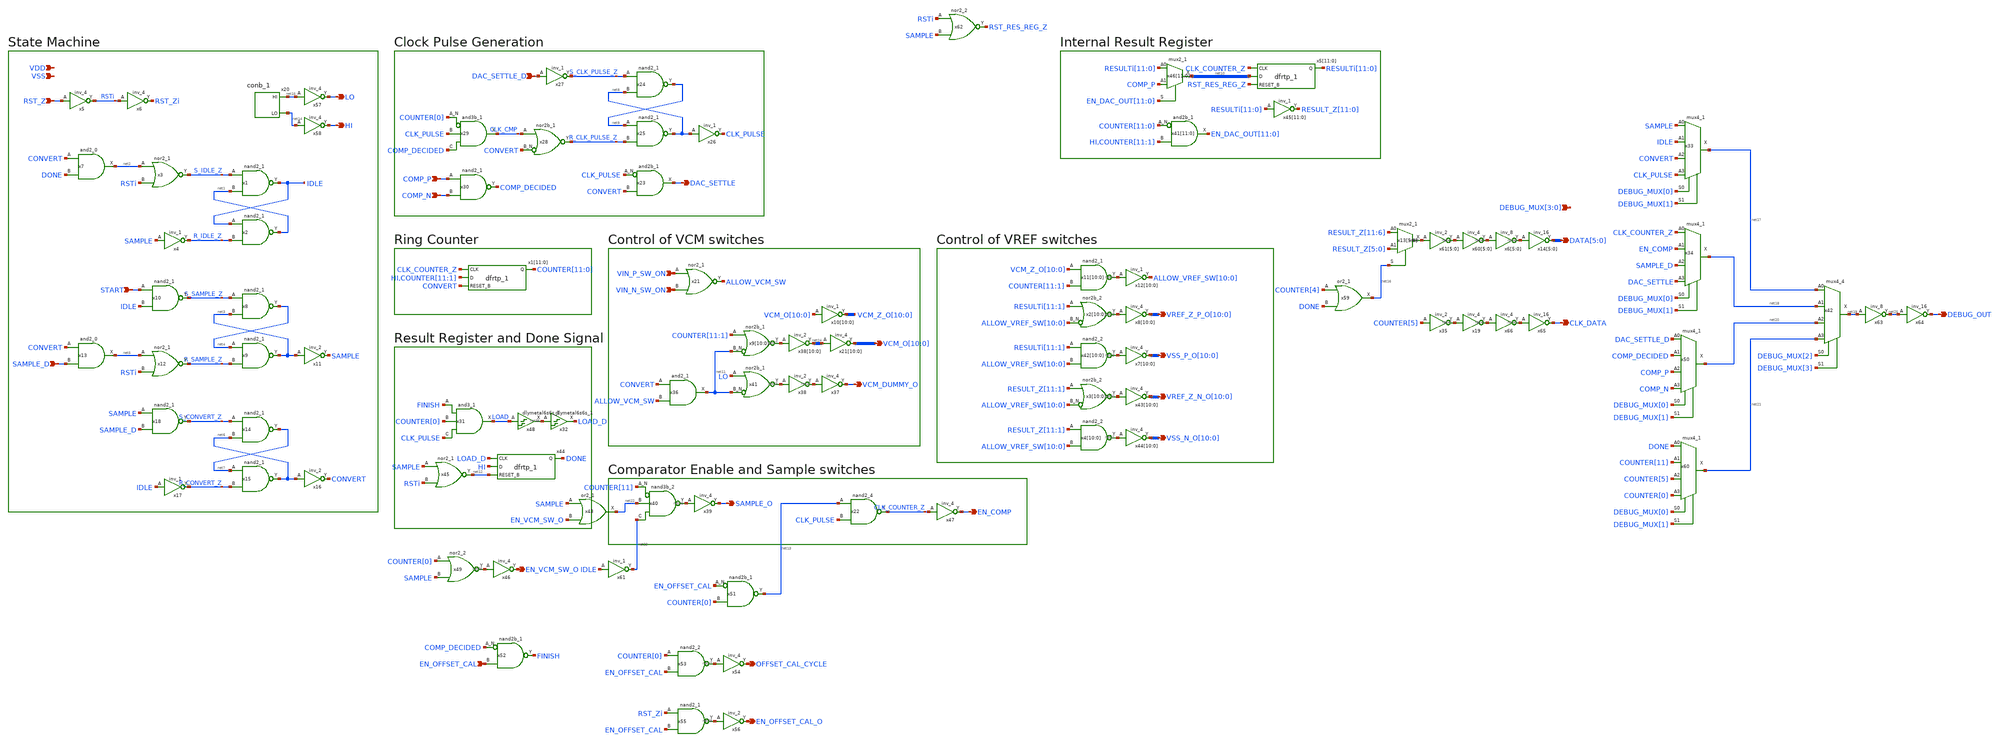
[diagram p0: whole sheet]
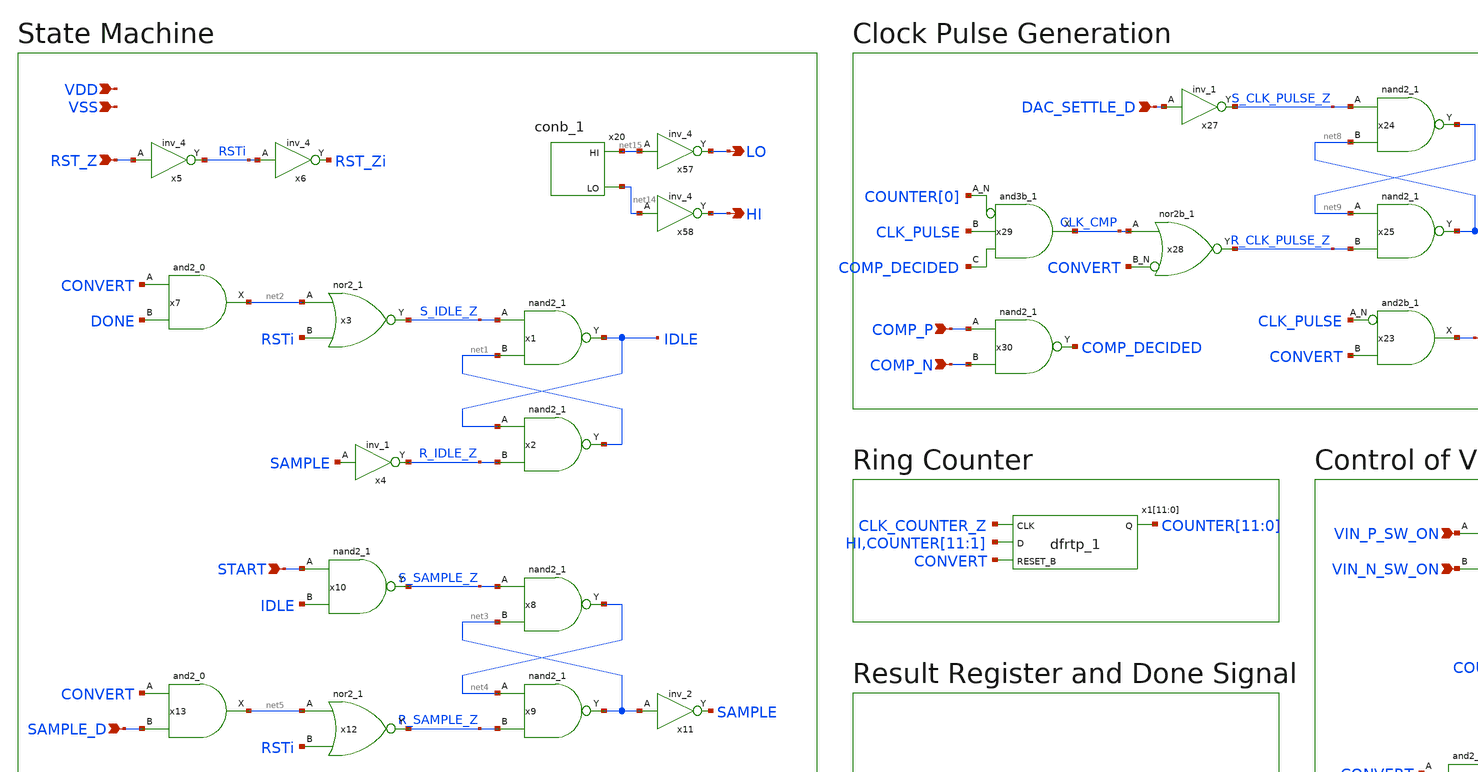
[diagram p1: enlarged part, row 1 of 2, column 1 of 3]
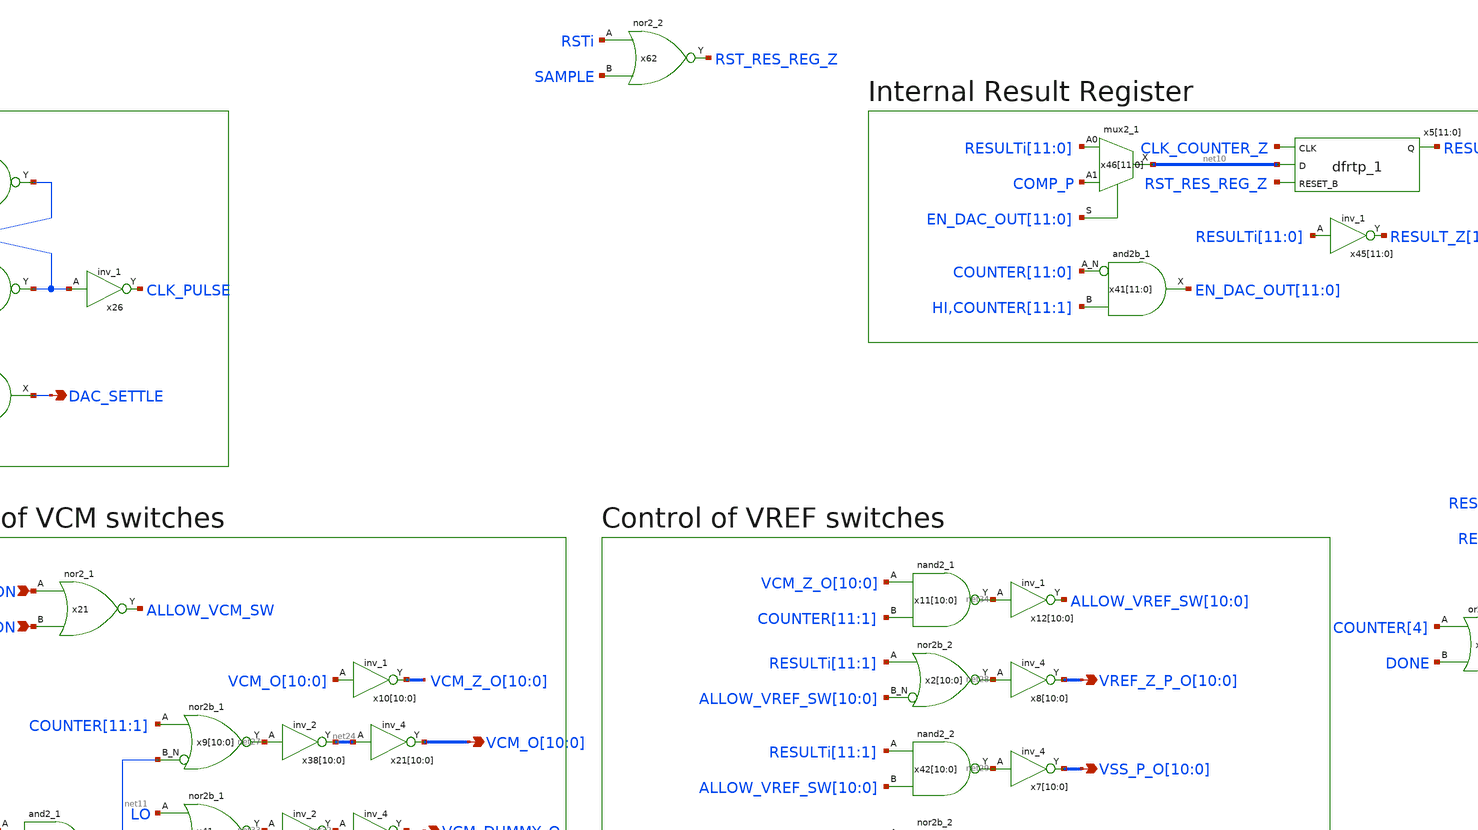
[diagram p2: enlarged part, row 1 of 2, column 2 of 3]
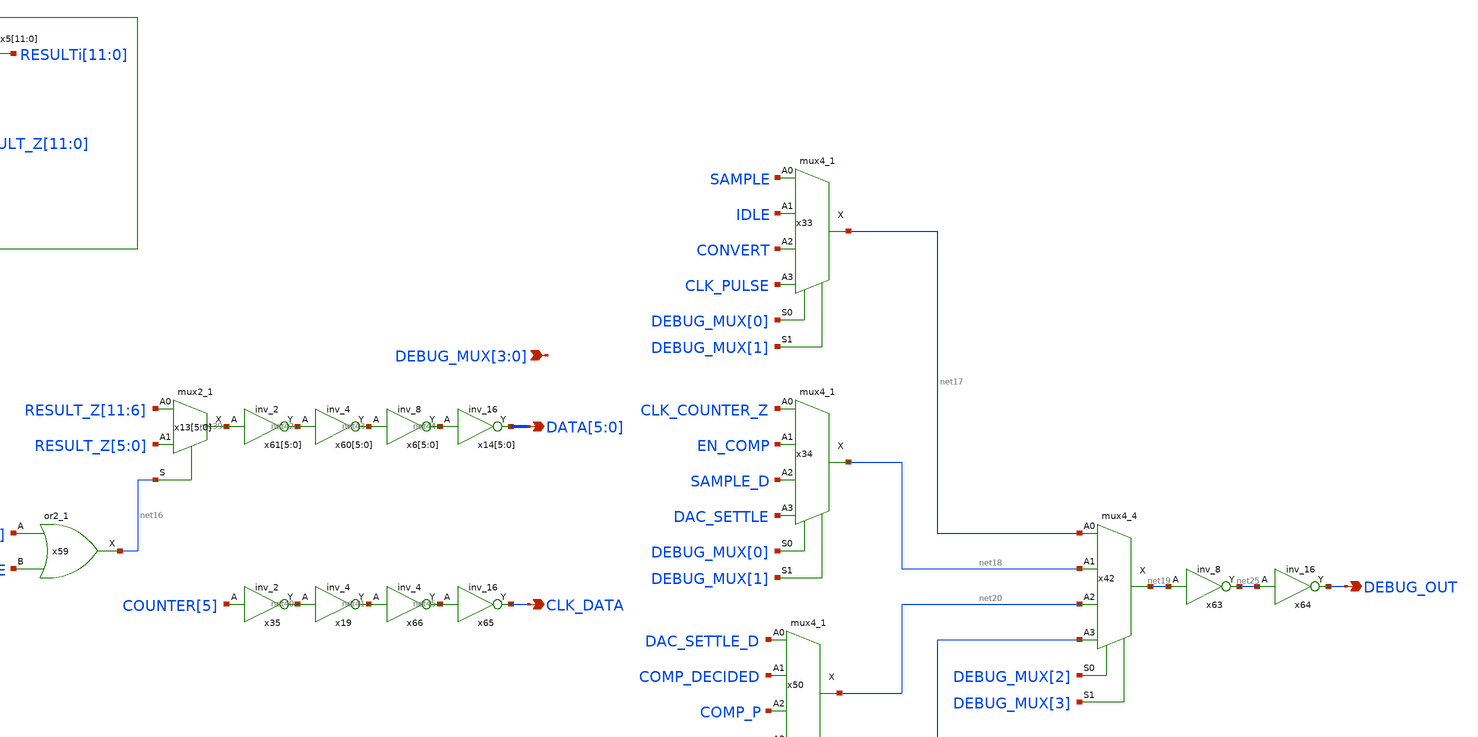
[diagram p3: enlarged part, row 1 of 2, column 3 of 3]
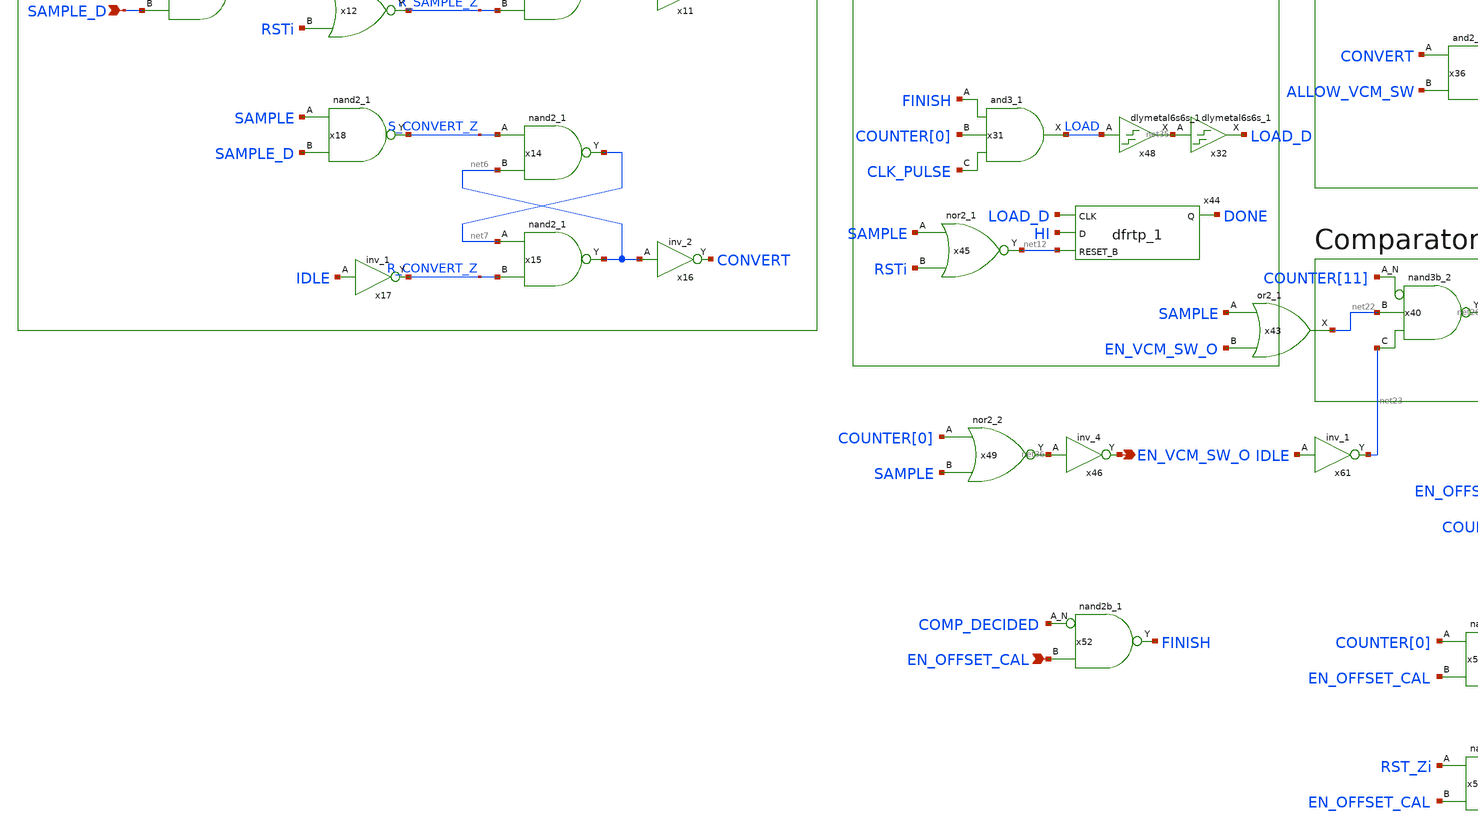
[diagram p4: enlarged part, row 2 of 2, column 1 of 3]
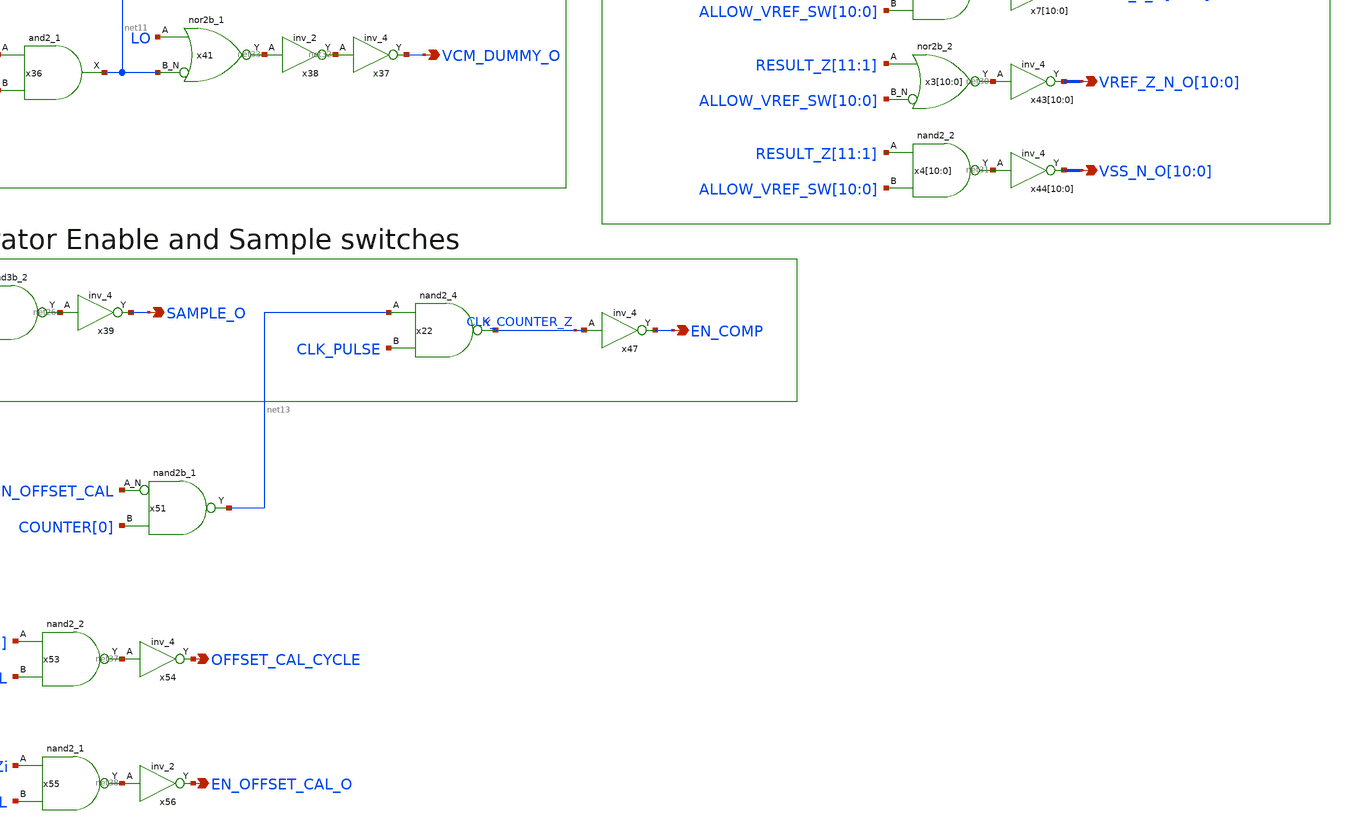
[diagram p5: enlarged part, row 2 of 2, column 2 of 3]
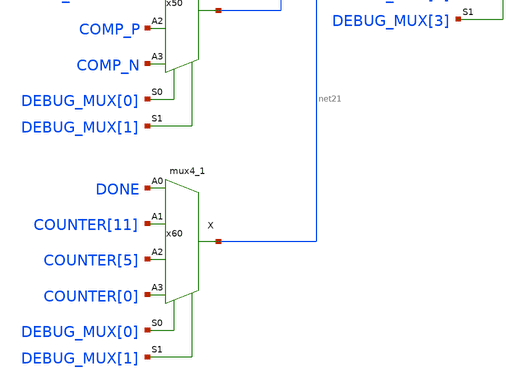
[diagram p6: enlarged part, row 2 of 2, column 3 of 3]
** sch_path: state_machine/openlane_backup/state_machine.sch
**.subckt state_machine RST_Z START COMP_P COMP_N SAMPLE_O
*+ VCM_O[10],VCM_O[9],VCM_O[8],VCM_O[7],VCM_O[6],VCM_O[5],VCM_O[4],VCM_O[3],VCM_O[2],VCM_O[1],VCM_O[0] EN_COMP VDD VSS VIN_P_SW_ON VIN_N_SW_ON VCM_DUMMY_O HI LO EN_VCM_SW_O EN_OFFSET_CAL
*+ OFFSET_CAL_CYCLE EN_OFFSET_CAL_O DAC_SETTLE DAC_SETTLE_D SAMPLE_D CLK_DATA
*+ DATA[5],DATA[4],DATA[3],DATA[2],DATA[1],DATA[0] DEBUG_OUT DEBUG_MUX[3],DEBUG_MUX[2],DEBUG_MUX[1],DEBUG_MUX[0]
*+ VREF_Z_P_O[10],VREF_Z_P_O[9],VREF_Z_P_O[8],VREF_Z_P_O[7],VREF_Z_P_O[6],VREF_Z_P_O[5],VREF_Z_P_O[4],VREF_Z_P_O[3],VREF_Z_P_O[2],VREF_Z_P_O[1],VREF_Z_P_O[0]
*+ VSS_P_O[10],VSS_P_O[9],VSS_P_O[8],VSS_P_O[7],VSS_P_O[6],VSS_P_O[5],VSS_P_O[4],VSS_P_O[3],VSS_P_O[2],VSS_P_O[1],VSS_P_O[0]
*+ VREF_Z_N_O[10],VREF_Z_N_O[9],VREF_Z_N_O[8],VREF_Z_N_O[7],VREF_Z_N_O[6],VREF_Z_N_O[5],VREF_Z_N_O[4],VREF_Z_N_O[3],VREF_Z_N_O[2],VREF_Z_N_O[1],VREF_Z_N_O[0]
*+ VSS_N_O[10],VSS_N_O[9],VSS_N_O[8],VSS_N_O[7],VSS_N_O[6],VSS_N_O[5],VSS_N_O[4],VSS_N_O[3],VSS_N_O[2],VSS_N_O[1],VSS_N_O[0]
*.ipin RST_Z
*.ipin START
*.ipin COMP_P
*.ipin COMP_N
*.opin SAMPLE_O
*.opin
*+ VCM_O[10],VCM_O[9],VCM_O[8],VCM_O[7],VCM_O[6],VCM_O[5],VCM_O[4],VCM_O[3],VCM_O[2],VCM_O[1],VCM_O[0]
*.opin EN_COMP
*.ipin VDD
*.ipin VSS
*.ipin VIN_P_SW_ON
*.ipin VIN_N_SW_ON
*.opin VCM_DUMMY_O
*.opin HI
*.opin LO
*.opin EN_VCM_SW_O
*.ipin EN_OFFSET_CAL
*.opin OFFSET_CAL_CYCLE
*.opin EN_OFFSET_CAL_O
*.opin DAC_SETTLE
*.ipin DAC_SETTLE_D
*.ipin SAMPLE_D
*.opin CLK_DATA
*.opin DATA[5],DATA[4],DATA[3],DATA[2],DATA[1],DATA[0]
*.opin DEBUG_OUT
*.ipin DEBUG_MUX[3],DEBUG_MUX[2],DEBUG_MUX[1],DEBUG_MUX[0]
*.opin
*+ VREF_Z_P_O[10],VREF_Z_P_O[9],VREF_Z_P_O[8],VREF_Z_P_O[7],VREF_Z_P_O[6],VREF_Z_P_O[5],VREF_Z_P_O[4],VREF_Z_P_O[3],VREF_Z_P_O[2],VREF_Z_P_O[1],VREF_Z_P_O[0]
*.opin
*+ VSS_P_O[10],VSS_P_O[9],VSS_P_O[8],VSS_P_O[7],VSS_P_O[6],VSS_P_O[5],VSS_P_O[4],VSS_P_O[3],VSS_P_O[2],VSS_P_O[1],VSS_P_O[0]
*.opin
*+ VREF_Z_N_O[10],VREF_Z_N_O[9],VREF_Z_N_O[8],VREF_Z_N_O[7],VREF_Z_N_O[6],VREF_Z_N_O[5],VREF_Z_N_O[4],VREF_Z_N_O[3],VREF_Z_N_O[2],VREF_Z_N_O[1],VREF_Z_N_O[0]
*.opin
*+ VSS_N_O[10],VSS_N_O[9],VSS_N_O[8],VSS_N_O[7],VSS_N_O[6],VSS_N_O[5],VSS_N_O[4],VSS_N_O[3],VSS_N_O[2],VSS_N_O[1],VSS_N_O[0]
x1 S_IDLE_Z net1 VSS VSS VDD VDD IDLE sky130_fd_sc_hd__nand2_1
x3 net2 RSTi VSS VSS VDD VDD S_IDLE_Z sky130_fd_sc_hd__nor2_1
x2 IDLE R_IDLE_Z VSS VSS VDD VDD net1 sky130_fd_sc_hd__nand2_1
x4 SAMPLE VSS VSS VDD VDD R_IDLE_Z sky130_fd_sc_hd__inv_1
x5 RST_Z VSS VSS VDD VDD RSTi sky130_fd_sc_hd__inv_4
x6 RSTi VSS VSS VDD VDD RST_Zi sky130_fd_sc_hd__inv_4
x7 CONVERT DONE VSS VSS VDD VDD net2 sky130_fd_sc_hd__and2_0
x8 S_SAMPLE_Z net3 VSS VSS VDD VDD net4 sky130_fd_sc_hd__nand2_1
x9 net4 R_SAMPLE_Z VSS VSS VDD VDD net3 sky130_fd_sc_hd__nand2_1
x10 START IDLE VSS VSS VDD VDD S_SAMPLE_Z sky130_fd_sc_hd__nand2_1
x11 net3 VSS VSS VDD VDD SAMPLE sky130_fd_sc_hd__inv_2
x12 net5 RSTi VSS VSS VDD VDD R_SAMPLE_Z sky130_fd_sc_hd__nor2_1
x13 CONVERT SAMPLE_D VSS VSS VDD VDD net5 sky130_fd_sc_hd__and2_0
x14 S_CONVERT_Z net6 VSS VSS VDD VDD net7 sky130_fd_sc_hd__nand2_1
x15 net7 R_CONVERT_Z VSS VSS VDD VDD net6 sky130_fd_sc_hd__nand2_1
x16 net6 VSS VSS VDD VDD CONVERT sky130_fd_sc_hd__inv_2
x17 IDLE VSS VSS VDD VDD R_CONVERT_Z sky130_fd_sc_hd__inv_1
x20 VSS VSS VDD VDD net15 net14 sky130_fd_sc_hd__conb_1
x23 CLK_PULSE CONVERT VSS VSS VDD VDD DAC_SETTLE sky130_fd_sc_hd__and2b_1
x24 S_CLK_PULSE_Z net8 VSS VSS VDD VDD net9 sky130_fd_sc_hd__nand2_1
x25 net9 R_CLK_PULSE_Z VSS VSS VDD VDD net8 sky130_fd_sc_hd__nand2_1
x26 net8 VSS VSS VDD VDD CLK_PULSE sky130_fd_sc_hd__inv_1
x27 DAC_SETTLE_D VSS VSS VDD VDD S_CLK_PULSE_Z sky130_fd_sc_hd__inv_1
x28 CLK_CMP CONVERT VSS VSS VDD VDD R_CLK_PULSE_Z sky130_fd_sc_hd__nor2b_1
x29 COUNTER[0] CLK_PULSE COMP_DECIDED VSS VSS VDD VDD CLK_CMP sky130_fd_sc_hd__and3b_1
x30 COMP_P COMP_N VSS VSS VDD VDD COMP_DECIDED sky130_fd_sc_hd__nand2_1
x39 net26 VSS VSS VDD VDD SAMPLE_O sky130_fd_sc_hd__inv_4
x40 COUNTER[11] net22 net23 VSS VSS VDD VDD net26 sky130_fd_sc_hd__nand3b_2
x1[11] CLK_COUNTER_Z HI CONVERT VSS VSS VDD VDD COUNTER[11] sky130_fd_sc_hd__dfrtp_1
x1[10] CLK_COUNTER_Z COUNTER[11] CONVERT VSS VSS VDD VDD COUNTER[10] sky130_fd_sc_hd__dfrtp_1
x1[9] CLK_COUNTER_Z COUNTER[10] CONVERT VSS VSS VDD VDD COUNTER[9] sky130_fd_sc_hd__dfrtp_1
x1[8] CLK_COUNTER_Z COUNTER[9] CONVERT VSS VSS VDD VDD COUNTER[8] sky130_fd_sc_hd__dfrtp_1
x1[7] CLK_COUNTER_Z COUNTER[8] CONVERT VSS VSS VDD VDD COUNTER[7] sky130_fd_sc_hd__dfrtp_1
x1[6] CLK_COUNTER_Z COUNTER[7] CONVERT VSS VSS VDD VDD COUNTER[6] sky130_fd_sc_hd__dfrtp_1
x1[5] CLK_COUNTER_Z COUNTER[6] CONVERT VSS VSS VDD VDD COUNTER[5] sky130_fd_sc_hd__dfrtp_1
x1[4] CLK_COUNTER_Z COUNTER[5] CONVERT VSS VSS VDD VDD COUNTER[4] sky130_fd_sc_hd__dfrtp_1
x1[3] CLK_COUNTER_Z COUNTER[4] CONVERT VSS VSS VDD VDD COUNTER[3] sky130_fd_sc_hd__dfrtp_1
x1[2] CLK_COUNTER_Z COUNTER[3] CONVERT VSS VSS VDD VDD COUNTER[2] sky130_fd_sc_hd__dfrtp_1
x1[1] CLK_COUNTER_Z COUNTER[2] CONVERT VSS VSS VDD VDD COUNTER[1] sky130_fd_sc_hd__dfrtp_1
x1[0] CLK_COUNTER_Z COUNTER[1] CONVERT VSS VSS VDD VDD COUNTER[0] sky130_fd_sc_hd__dfrtp_1
x21[10] net24[10] VSS VSS VDD VDD VCM_O[10] sky130_fd_sc_hd__inv_4
x21[9] net24[9] VSS VSS VDD VDD VCM_O[9] sky130_fd_sc_hd__inv_4
x21[8] net24[8] VSS VSS VDD VDD VCM_O[8] sky130_fd_sc_hd__inv_4
x21[7] net24[7] VSS VSS VDD VDD VCM_O[7] sky130_fd_sc_hd__inv_4
x21[6] net24[6] VSS VSS VDD VDD VCM_O[6] sky130_fd_sc_hd__inv_4
x21[5] net24[5] VSS VSS VDD VDD VCM_O[5] sky130_fd_sc_hd__inv_4
x21[4] net24[4] VSS VSS VDD VDD VCM_O[4] sky130_fd_sc_hd__inv_4
x21[3] net24[3] VSS VSS VDD VDD VCM_O[3] sky130_fd_sc_hd__inv_4
x21[2] net24[2] VSS VSS VDD VDD VCM_O[2] sky130_fd_sc_hd__inv_4
x21[1] net24[1] VSS VSS VDD VDD VCM_O[1] sky130_fd_sc_hd__inv_4
x21[0] net24[0] VSS VSS VDD VDD VCM_O[0] sky130_fd_sc_hd__inv_4
x38[10] net27[10] VSS VSS VDD VDD net24[10] sky130_fd_sc_hd__inv_2
x38[9] net27[9] VSS VSS VDD VDD net24[9] sky130_fd_sc_hd__inv_2
x38[8] net27[8] VSS VSS VDD VDD net24[8] sky130_fd_sc_hd__inv_2
x38[7] net27[7] VSS VSS VDD VDD net24[7] sky130_fd_sc_hd__inv_2
x38[6] net27[6] VSS VSS VDD VDD net24[6] sky130_fd_sc_hd__inv_2
x38[5] net27[5] VSS VSS VDD VDD net24[5] sky130_fd_sc_hd__inv_2
x38[4] net27[4] VSS VSS VDD VDD net24[4] sky130_fd_sc_hd__inv_2
x38[3] net27[3] VSS VSS VDD VDD net24[3] sky130_fd_sc_hd__inv_2
x38[2] net27[2] VSS VSS VDD VDD net24[2] sky130_fd_sc_hd__inv_2
x38[1] net27[1] VSS VSS VDD VDD net24[1] sky130_fd_sc_hd__inv_2
x38[0] net27[0] VSS VSS VDD VDD net24[0] sky130_fd_sc_hd__inv_2
x41[11] COUNTER[11] HI VSS VSS VDD VDD EN_DAC_OUT[11] sky130_fd_sc_hd__and2b_1
x41[10] COUNTER[10] COUNTER[11] VSS VSS VDD VDD EN_DAC_OUT[10] sky130_fd_sc_hd__and2b_1
x41[9] COUNTER[9] COUNTER[10] VSS VSS VDD VDD EN_DAC_OUT[9] sky130_fd_sc_hd__and2b_1
x41[8] COUNTER[8] COUNTER[9] VSS VSS VDD VDD EN_DAC_OUT[8] sky130_fd_sc_hd__and2b_1
x41[7] COUNTER[7] COUNTER[8] VSS VSS VDD VDD EN_DAC_OUT[7] sky130_fd_sc_hd__and2b_1
x41[6] COUNTER[6] COUNTER[7] VSS VSS VDD VDD EN_DAC_OUT[6] sky130_fd_sc_hd__and2b_1
x41[5] COUNTER[5] COUNTER[6] VSS VSS VDD VDD EN_DAC_OUT[5] sky130_fd_sc_hd__and2b_1
x41[4] COUNTER[4] COUNTER[5] VSS VSS VDD VDD EN_DAC_OUT[4] sky130_fd_sc_hd__and2b_1
x41[3] COUNTER[3] COUNTER[4] VSS VSS VDD VDD EN_DAC_OUT[3] sky130_fd_sc_hd__and2b_1
x41[2] COUNTER[2] COUNTER[3] VSS VSS VDD VDD EN_DAC_OUT[2] sky130_fd_sc_hd__and2b_1
x41[1] COUNTER[1] COUNTER[2] VSS VSS VDD VDD EN_DAC_OUT[1] sky130_fd_sc_hd__and2b_1
x41[0] COUNTER[0] COUNTER[1] VSS VSS VDD VDD EN_DAC_OUT[0] sky130_fd_sc_hd__and2b_1
x2[10] RESULTi[11] ALLOW_VREF_SW[10] VSS VSS VDD VDD net28[10] sky130_fd_sc_hd__nor2b_2
x2[9] RESULTi[10] ALLOW_VREF_SW[9] VSS VSS VDD VDD net28[9] sky130_fd_sc_hd__nor2b_2
x2[8] RESULTi[9] ALLOW_VREF_SW[8] VSS VSS VDD VDD net28[8] sky130_fd_sc_hd__nor2b_2
x2[7] RESULTi[8] ALLOW_VREF_SW[7] VSS VSS VDD VDD net28[7] sky130_fd_sc_hd__nor2b_2
x2[6] RESULTi[7] ALLOW_VREF_SW[6] VSS VSS VDD VDD net28[6] sky130_fd_sc_hd__nor2b_2
x2[5] RESULTi[6] ALLOW_VREF_SW[5] VSS VSS VDD VDD net28[5] sky130_fd_sc_hd__nor2b_2
x2[4] RESULTi[5] ALLOW_VREF_SW[4] VSS VSS VDD VDD net28[4] sky130_fd_sc_hd__nor2b_2
x2[3] RESULTi[4] ALLOW_VREF_SW[3] VSS VSS VDD VDD net28[3] sky130_fd_sc_hd__nor2b_2
x2[2] RESULTi[3] ALLOW_VREF_SW[2] VSS VSS VDD VDD net28[2] sky130_fd_sc_hd__nor2b_2
x2[1] RESULTi[2] ALLOW_VREF_SW[1] VSS VSS VDD VDD net28[1] sky130_fd_sc_hd__nor2b_2
x2[0] RESULTi[1] ALLOW_VREF_SW[0] VSS VSS VDD VDD net28[0] sky130_fd_sc_hd__nor2b_2
x8[10] net28[10] VSS VSS VDD VDD VREF_Z_P_O[10] sky130_fd_sc_hd__inv_4
x8[9] net28[9] VSS VSS VDD VDD VREF_Z_P_O[9] sky130_fd_sc_hd__inv_4
x8[8] net28[8] VSS VSS VDD VDD VREF_Z_P_O[8] sky130_fd_sc_hd__inv_4
x8[7] net28[7] VSS VSS VDD VDD VREF_Z_P_O[7] sky130_fd_sc_hd__inv_4
x8[6] net28[6] VSS VSS VDD VDD VREF_Z_P_O[6] sky130_fd_sc_hd__inv_4
x8[5] net28[5] VSS VSS VDD VDD VREF_Z_P_O[5] sky130_fd_sc_hd__inv_4
x8[4] net28[4] VSS VSS VDD VDD VREF_Z_P_O[4] sky130_fd_sc_hd__inv_4
x8[3] net28[3] VSS VSS VDD VDD VREF_Z_P_O[3] sky130_fd_sc_hd__inv_4
x8[2] net28[2] VSS VSS VDD VDD VREF_Z_P_O[2] sky130_fd_sc_hd__inv_4
x8[1] net28[1] VSS VSS VDD VDD VREF_Z_P_O[1] sky130_fd_sc_hd__inv_4
x8[0] net28[0] VSS VSS VDD VDD VREF_Z_P_O[0] sky130_fd_sc_hd__inv_4
x42[10] RESULTi[11] ALLOW_VREF_SW[10] VSS VSS VDD VDD net29[10] sky130_fd_sc_hd__nand2_2
x42[9] RESULTi[10] ALLOW_VREF_SW[9] VSS VSS VDD VDD net29[9] sky130_fd_sc_hd__nand2_2
x42[8] RESULTi[9] ALLOW_VREF_SW[8] VSS VSS VDD VDD net29[8] sky130_fd_sc_hd__nand2_2
x42[7] RESULTi[8] ALLOW_VREF_SW[7] VSS VSS VDD VDD net29[7] sky130_fd_sc_hd__nand2_2
x42[6] RESULTi[7] ALLOW_VREF_SW[6] VSS VSS VDD VDD net29[6] sky130_fd_sc_hd__nand2_2
x42[5] RESULTi[6] ALLOW_VREF_SW[5] VSS VSS VDD VDD net29[5] sky130_fd_sc_hd__nand2_2
x42[4] RESULTi[5] ALLOW_VREF_SW[4] VSS VSS VDD VDD net29[4] sky130_fd_sc_hd__nand2_2
x42[3] RESULTi[4] ALLOW_VREF_SW[3] VSS VSS VDD VDD net29[3] sky130_fd_sc_hd__nand2_2
x42[2] RESULTi[3] ALLOW_VREF_SW[2] VSS VSS VDD VDD net29[2] sky130_fd_sc_hd__nand2_2
x42[1] RESULTi[2] ALLOW_VREF_SW[1] VSS VSS VDD VDD net29[1] sky130_fd_sc_hd__nand2_2
x42[0] RESULTi[1] ALLOW_VREF_SW[0] VSS VSS VDD VDD net29[0] sky130_fd_sc_hd__nand2_2
x7[10] net29[10] VSS VSS VDD VDD VSS_P_O[10] sky130_fd_sc_hd__inv_4
x7[9] net29[9] VSS VSS VDD VDD VSS_P_O[9] sky130_fd_sc_hd__inv_4
x7[8] net29[8] VSS VSS VDD VDD VSS_P_O[8] sky130_fd_sc_hd__inv_4
x7[7] net29[7] VSS VSS VDD VDD VSS_P_O[7] sky130_fd_sc_hd__inv_4
x7[6] net29[6] VSS VSS VDD VDD VSS_P_O[6] sky130_fd_sc_hd__inv_4
x7[5] net29[5] VSS VSS VDD VDD VSS_P_O[5] sky130_fd_sc_hd__inv_4
x7[4] net29[4] VSS VSS VDD VDD VSS_P_O[4] sky130_fd_sc_hd__inv_4
x7[3] net29[3] VSS VSS VDD VDD VSS_P_O[3] sky130_fd_sc_hd__inv_4
x7[2] net29[2] VSS VSS VDD VDD VSS_P_O[2] sky130_fd_sc_hd__inv_4
x7[1] net29[1] VSS VSS VDD VDD VSS_P_O[1] sky130_fd_sc_hd__inv_4
x7[0] net29[0] VSS VSS VDD VDD VSS_P_O[0] sky130_fd_sc_hd__inv_4
x3[10] RESULT_Z[11] ALLOW_VREF_SW[10] VSS VSS VDD VDD net30[10] sky130_fd_sc_hd__nor2b_2
x3[9] RESULT_Z[10] ALLOW_VREF_SW[9] VSS VSS VDD VDD net30[9] sky130_fd_sc_hd__nor2b_2
x3[8] RESULT_Z[9] ALLOW_VREF_SW[8] VSS VSS VDD VDD net30[8] sky130_fd_sc_hd__nor2b_2
x3[7] RESULT_Z[8] ALLOW_VREF_SW[7] VSS VSS VDD VDD net30[7] sky130_fd_sc_hd__nor2b_2
x3[6] RESULT_Z[7] ALLOW_VREF_SW[6] VSS VSS VDD VDD net30[6] sky130_fd_sc_hd__nor2b_2
x3[5] RESULT_Z[6] ALLOW_VREF_SW[5] VSS VSS VDD VDD net30[5] sky130_fd_sc_hd__nor2b_2
x3[4] RESULT_Z[5] ALLOW_VREF_SW[4] VSS VSS VDD VDD net30[4] sky130_fd_sc_hd__nor2b_2
x3[3] RESULT_Z[4] ALLOW_VREF_SW[3] VSS VSS VDD VDD net30[3] sky130_fd_sc_hd__nor2b_2
x3[2] RESULT_Z[3] ALLOW_VREF_SW[2] VSS VSS VDD VDD net30[2] sky130_fd_sc_hd__nor2b_2
x3[1] RESULT_Z[2] ALLOW_VREF_SW[1] VSS VSS VDD VDD net30[1] sky130_fd_sc_hd__nor2b_2
x3[0] RESULT_Z[1] ALLOW_VREF_SW[0] VSS VSS VDD VDD net30[0] sky130_fd_sc_hd__nor2b_2
x43[10] net30[10] VSS VSS VDD VDD VREF_Z_N_O[10] sky130_fd_sc_hd__inv_4
x43[9] net30[9] VSS VSS VDD VDD VREF_Z_N_O[9] sky130_fd_sc_hd__inv_4
x43[8] net30[8] VSS VSS VDD VDD VREF_Z_N_O[8] sky130_fd_sc_hd__inv_4
x43[7] net30[7] VSS VSS VDD VDD VREF_Z_N_O[7] sky130_fd_sc_hd__inv_4
x43[6] net30[6] VSS VSS VDD VDD VREF_Z_N_O[6] sky130_fd_sc_hd__inv_4
x43[5] net30[5] VSS VSS VDD VDD VREF_Z_N_O[5] sky130_fd_sc_hd__inv_4
x43[4] net30[4] VSS VSS VDD VDD VREF_Z_N_O[4] sky130_fd_sc_hd__inv_4
x43[3] net30[3] VSS VSS VDD VDD VREF_Z_N_O[3] sky130_fd_sc_hd__inv_4
x43[2] net30[2] VSS VSS VDD VDD VREF_Z_N_O[2] sky130_fd_sc_hd__inv_4
x43[1] net30[1] VSS VSS VDD VDD VREF_Z_N_O[1] sky130_fd_sc_hd__inv_4
x43[0] net30[0] VSS VSS VDD VDD VREF_Z_N_O[0] sky130_fd_sc_hd__inv_4
x4[10] RESULT_Z[11] ALLOW_VREF_SW[10] VSS VSS VDD VDD net31[10] sky130_fd_sc_hd__nand2_2
x4[9] RESULT_Z[10] ALLOW_VREF_SW[9] VSS VSS VDD VDD net31[9] sky130_fd_sc_hd__nand2_2
x4[8] RESULT_Z[9] ALLOW_VREF_SW[8] VSS VSS VDD VDD net31[8] sky130_fd_sc_hd__nand2_2
x4[7] RESULT_Z[8] ALLOW_VREF_SW[7] VSS VSS VDD VDD net31[7] sky130_fd_sc_hd__nand2_2
x4[6] RESULT_Z[7] ALLOW_VREF_SW[6] VSS VSS VDD VDD net31[6] sky130_fd_sc_hd__nand2_2
x4[5] RESULT_Z[6] ALLOW_VREF_SW[5] VSS VSS VDD VDD net31[5] sky130_fd_sc_hd__nand2_2
x4[4] RESULT_Z[5] ALLOW_VREF_SW[4] VSS VSS VDD VDD net31[4] sky130_fd_sc_hd__nand2_2
x4[3] RESULT_Z[4] ALLOW_VREF_SW[3] VSS VSS VDD VDD net31[3] sky130_fd_sc_hd__nand2_2
x4[2] RESULT_Z[3] ALLOW_VREF_SW[2] VSS VSS VDD VDD net31[2] sky130_fd_sc_hd__nand2_2
x4[1] RESULT_Z[2] ALLOW_VREF_SW[1] VSS VSS VDD VDD net31[1] sky130_fd_sc_hd__nand2_2
x4[0] RESULT_Z[1] ALLOW_VREF_SW[0] VSS VSS VDD VDD net31[0] sky130_fd_sc_hd__nand2_2
x44[10] net31[10] VSS VSS VDD VDD VSS_N_O[10] sky130_fd_sc_hd__inv_4
x44[9] net31[9] VSS VSS VDD VDD VSS_N_O[9] sky130_fd_sc_hd__inv_4
x44[8] net31[8] VSS VSS VDD VDD VSS_N_O[8] sky130_fd_sc_hd__inv_4
x44[7] net31[7] VSS VSS VDD VDD VSS_N_O[7] sky130_fd_sc_hd__inv_4
x44[6] net31[6] VSS VSS VDD VDD VSS_N_O[6] sky130_fd_sc_hd__inv_4
x44[5] net31[5] VSS VSS VDD VDD VSS_N_O[5] sky130_fd_sc_hd__inv_4
x44[4] net31[4] VSS VSS VDD VDD VSS_N_O[4] sky130_fd_sc_hd__inv_4
x44[3] net31[3] VSS VSS VDD VDD VSS_N_O[3] sky130_fd_sc_hd__inv_4
x44[2] net31[2] VSS VSS VDD VDD VSS_N_O[2] sky130_fd_sc_hd__inv_4
x44[1] net31[1] VSS VSS VDD VDD VSS_N_O[1] sky130_fd_sc_hd__inv_4
x44[0] net31[0] VSS VSS VDD VDD VSS_N_O[0] sky130_fd_sc_hd__inv_4
x45[11] RESULTi[11] VSS VSS VDD VDD RESULT_Z[11] sky130_fd_sc_hd__inv_1
x45[10] RESULTi[10] VSS VSS VDD VDD RESULT_Z[10] sky130_fd_sc_hd__inv_1
x45[9] RESULTi[9] VSS VSS VDD VDD RESULT_Z[9] sky130_fd_sc_hd__inv_1
x45[8] RESULTi[8] VSS VSS VDD VDD RESULT_Z[8] sky130_fd_sc_hd__inv_1
x45[7] RESULTi[7] VSS VSS VDD VDD RESULT_Z[7] sky130_fd_sc_hd__inv_1
x45[6] RESULTi[6] VSS VSS VDD VDD RESULT_Z[6] sky130_fd_sc_hd__inv_1
x45[5] RESULTi[5] VSS VSS VDD VDD RESULT_Z[5] sky130_fd_sc_hd__inv_1
x45[4] RESULTi[4] VSS VSS VDD VDD RESULT_Z[4] sky130_fd_sc_hd__inv_1
x45[3] RESULTi[3] VSS VSS VDD VDD RESULT_Z[3] sky130_fd_sc_hd__inv_1
x45[2] RESULTi[2] VSS VSS VDD VDD RESULT_Z[2] sky130_fd_sc_hd__inv_1
x45[1] RESULTi[1] VSS VSS VDD VDD RESULT_Z[1] sky130_fd_sc_hd__inv_1
x45[0] RESULTi[0] VSS VSS VDD VDD RESULT_Z[0] sky130_fd_sc_hd__inv_1
x5[11] CLK_COUNTER_Z net10[11] RST_RES_REG_Z VSS VSS VDD VDD RESULTi[11] sky130_fd_sc_hd__dfrtp_1
x5[10] CLK_COUNTER_Z net10[10] RST_RES_REG_Z VSS VSS VDD VDD RESULTi[10] sky130_fd_sc_hd__dfrtp_1
x5[9] CLK_COUNTER_Z net10[9] RST_RES_REG_Z VSS VSS VDD VDD RESULTi[9] sky130_fd_sc_hd__dfrtp_1
x5[8] CLK_COUNTER_Z net10[8] RST_RES_REG_Z VSS VSS VDD VDD RESULTi[8] sky130_fd_sc_hd__dfrtp_1
x5[7] CLK_COUNTER_Z net10[7] RST_RES_REG_Z VSS VSS VDD VDD RESULTi[7] sky130_fd_sc_hd__dfrtp_1
x5[6] CLK_COUNTER_Z net10[6] RST_RES_REG_Z VSS VSS VDD VDD RESULTi[6] sky130_fd_sc_hd__dfrtp_1
x5[5] CLK_COUNTER_Z net10[5] RST_RES_REG_Z VSS VSS VDD VDD RESULTi[5] sky130_fd_sc_hd__dfrtp_1
x5[4] CLK_COUNTER_Z net10[4] RST_RES_REG_Z VSS VSS VDD VDD RESULTi[4] sky130_fd_sc_hd__dfrtp_1
x5[3] CLK_COUNTER_Z net10[3] RST_RES_REG_Z VSS VSS VDD VDD RESULTi[3] sky130_fd_sc_hd__dfrtp_1
x5[2] CLK_COUNTER_Z net10[2] RST_RES_REG_Z VSS VSS VDD VDD RESULTi[2] sky130_fd_sc_hd__dfrtp_1
x5[1] CLK_COUNTER_Z net10[1] RST_RES_REG_Z VSS VSS VDD VDD RESULTi[1] sky130_fd_sc_hd__dfrtp_1
x5[0] CLK_COUNTER_Z net10[0] RST_RES_REG_Z VSS VSS VDD VDD RESULTi[0] sky130_fd_sc_hd__dfrtp_1
x46[11] RESULTi[11] COMP_P EN_DAC_OUT[11] VSS VSS VDD VDD net10[11] sky130_fd_sc_hd__mux2_1
x46[10] RESULTi[10] COMP_P EN_DAC_OUT[10] VSS VSS VDD VDD net10[10] sky130_fd_sc_hd__mux2_1
x46[9] RESULTi[9] COMP_P EN_DAC_OUT[9] VSS VSS VDD VDD net10[9] sky130_fd_sc_hd__mux2_1
x46[8] RESULTi[8] COMP_P EN_DAC_OUT[8] VSS VSS VDD VDD net10[8] sky130_fd_sc_hd__mux2_1
x46[7] RESULTi[7] COMP_P EN_DAC_OUT[7] VSS VSS VDD VDD net10[7] sky130_fd_sc_hd__mux2_1
x46[6] RESULTi[6] COMP_P EN_DAC_OUT[6] VSS VSS VDD VDD net10[6] sky130_fd_sc_hd__mux2_1
x46[5] RESULTi[5] COMP_P EN_DAC_OUT[5] VSS VSS VDD VDD net10[5] sky130_fd_sc_hd__mux2_1
x46[4] RESULTi[4] COMP_P EN_DAC_OUT[4] VSS VSS VDD VDD net10[4] sky130_fd_sc_hd__mux2_1
x46[3] RESULTi[3] COMP_P EN_DAC_OUT[3] VSS VSS VDD VDD net10[3] sky130_fd_sc_hd__mux2_1
x46[2] RESULTi[2] COMP_P EN_DAC_OUT[2] VSS VSS VDD VDD net10[2] sky130_fd_sc_hd__mux2_1
x46[1] RESULTi[1] COMP_P EN_DAC_OUT[1] VSS VSS VDD VDD net10[1] sky130_fd_sc_hd__mux2_1
x46[0] RESULTi[0] COMP_P EN_DAC_OUT[0] VSS VSS VDD VDD net10[0] sky130_fd_sc_hd__mux2_1
x47 CLK_COUNTER_Z VSS VSS VDD VDD EN_COMP sky130_fd_sc_hd__inv_4
x22 net13 CLK_PULSE VSS VSS VDD VDD CLK_COUNTER_Z sky130_fd_sc_hd__nand2_4
x31 FINISH COUNTER[0] CLK_PULSE VSS VSS VDD VDD LOAD sky130_fd_sc_hd__and3_1
x9[10] COUNTER[11] net11 VSS VSS VDD VDD net27[10] sky130_fd_sc_hd__nor2b_1
x9[9] COUNTER[10] net11 VSS VSS VDD VDD net27[9] sky130_fd_sc_hd__nor2b_1
x9[8] COUNTER[9] net11 VSS VSS VDD VDD net27[8] sky130_fd_sc_hd__nor2b_1
x9[7] COUNTER[8] net11 VSS VSS VDD VDD net27[7] sky130_fd_sc_hd__nor2b_1
x9[6] COUNTER[7] net11 VSS VSS VDD VDD net27[6] sky130_fd_sc_hd__nor2b_1
x9[5] COUNTER[6] net11 VSS VSS VDD VDD net27[5] sky130_fd_sc_hd__nor2b_1
x9[4] COUNTER[5] net11 VSS VSS VDD VDD net27[4] sky130_fd_sc_hd__nor2b_1
x9[3] COUNTER[4] net11 VSS VSS VDD VDD net27[3] sky130_fd_sc_hd__nor2b_1
x9[2] COUNTER[3] net11 VSS VSS VDD VDD net27[2] sky130_fd_sc_hd__nor2b_1
x9[1] COUNTER[2] net11 VSS VSS VDD VDD net27[1] sky130_fd_sc_hd__nor2b_1
x9[0] COUNTER[1] net11 VSS VSS VDD VDD net27[0] sky130_fd_sc_hd__nor2b_1
x18 SAMPLE SAMPLE_D VSS VSS VDD VDD S_CONVERT_Z sky130_fd_sc_hd__nand2_1
x21 VIN_P_SW_ON VIN_N_SW_ON VSS VSS VDD VDD ALLOW_VCM_SW sky130_fd_sc_hd__nor2_1
x36 CONVERT ALLOW_VCM_SW VSS VSS VDD VDD net11 sky130_fd_sc_hd__and2_1
x37 net32 VSS VSS VDD VDD VCM_DUMMY_O sky130_fd_sc_hd__inv_4
x38 net33 VSS VSS VDD VDD net32 sky130_fd_sc_hd__inv_2
x41 LO net11 VSS VSS VDD VDD net33 sky130_fd_sc_hd__nor2b_1
x44 LOAD_D HI net12 VSS VSS VDD VDD DONE sky130_fd_sc_hd__dfrtp_1
x10[10] VCM_O[10] VSS VSS VDD VDD VCM_Z_O[10] sky130_fd_sc_hd__inv_1
x10[9] VCM_O[9] VSS VSS VDD VDD VCM_Z_O[9] sky130_fd_sc_hd__inv_1
x10[8] VCM_O[8] VSS VSS VDD VDD VCM_Z_O[8] sky130_fd_sc_hd__inv_1
x10[7] VCM_O[7] VSS VSS VDD VDD VCM_Z_O[7] sky130_fd_sc_hd__inv_1
x10[6] VCM_O[6] VSS VSS VDD VDD VCM_Z_O[6] sky130_fd_sc_hd__inv_1
x10[5] VCM_O[5] VSS VSS VDD VDD VCM_Z_O[5] sky130_fd_sc_hd__inv_1
x10[4] VCM_O[4] VSS VSS VDD VDD VCM_Z_O[4] sky130_fd_sc_hd__inv_1
x10[3] VCM_O[3] VSS VSS VDD VDD VCM_Z_O[3] sky130_fd_sc_hd__inv_1
x10[2] VCM_O[2] VSS VSS VDD VDD VCM_Z_O[2] sky130_fd_sc_hd__inv_1
x10[1] VCM_O[1] VSS VSS VDD VDD VCM_Z_O[1] sky130_fd_sc_hd__inv_1
x10[0] VCM_O[0] VSS VSS VDD VDD VCM_Z_O[0] sky130_fd_sc_hd__inv_1
x11[10] VCM_Z_O[10] COUNTER[11] VSS VSS VDD VDD net34[10] sky130_fd_sc_hd__nand2_1
x11[9] VCM_Z_O[9] COUNTER[10] VSS VSS VDD VDD net34[9] sky130_fd_sc_hd__nand2_1
x11[8] VCM_Z_O[8] COUNTER[9] VSS VSS VDD VDD net34[8] sky130_fd_sc_hd__nand2_1
x11[7] VCM_Z_O[7] COUNTER[8] VSS VSS VDD VDD net34[7] sky130_fd_sc_hd__nand2_1
x11[6] VCM_Z_O[6] COUNTER[7] VSS VSS VDD VDD net34[6] sky130_fd_sc_hd__nand2_1
x11[5] VCM_Z_O[5] COUNTER[6] VSS VSS VDD VDD net34[5] sky130_fd_sc_hd__nand2_1
x11[4] VCM_Z_O[4] COUNTER[5] VSS VSS VDD VDD net34[4] sky130_fd_sc_hd__nand2_1
x11[3] VCM_Z_O[3] COUNTER[4] VSS VSS VDD VDD net34[3] sky130_fd_sc_hd__nand2_1
x11[2] VCM_Z_O[2] COUNTER[3] VSS VSS VDD VDD net34[2] sky130_fd_sc_hd__nand2_1
x11[1] VCM_Z_O[1] COUNTER[2] VSS VSS VDD VDD net34[1] sky130_fd_sc_hd__nand2_1
x11[0] VCM_Z_O[0] COUNTER[1] VSS VSS VDD VDD net34[0] sky130_fd_sc_hd__nand2_1
x45 SAMPLE RSTi VSS VSS VDD VDD net12 sky130_fd_sc_hd__nor2_1
x12[10] net34[10] VSS VSS VDD VDD ALLOW_VREF_SW[10] sky130_fd_sc_hd__inv_1
x12[9] net34[9] VSS VSS VDD VDD ALLOW_VREF_SW[9] sky130_fd_sc_hd__inv_1
x12[8] net34[8] VSS VSS VDD VDD ALLOW_VREF_SW[8] sky130_fd_sc_hd__inv_1
x12[7] net34[7] VSS VSS VDD VDD ALLOW_VREF_SW[7] sky130_fd_sc_hd__inv_1
x12[6] net34[6] VSS VSS VDD VDD ALLOW_VREF_SW[6] sky130_fd_sc_hd__inv_1
x12[5] net34[5] VSS VSS VDD VDD ALLOW_VREF_SW[5] sky130_fd_sc_hd__inv_1
x12[4] net34[4] VSS VSS VDD VDD ALLOW_VREF_SW[4] sky130_fd_sc_hd__inv_1
x12[3] net34[3] VSS VSS VDD VDD ALLOW_VREF_SW[3] sky130_fd_sc_hd__inv_1
x12[2] net34[2] VSS VSS VDD VDD ALLOW_VREF_SW[2] sky130_fd_sc_hd__inv_1
x12[1] net34[1] VSS VSS VDD VDD ALLOW_VREF_SW[1] sky130_fd_sc_hd__inv_1
x12[0] net34[0] VSS VSS VDD VDD ALLOW_VREF_SW[0] sky130_fd_sc_hd__inv_1
x48 LOAD VSS VSS VDD VDD net35 sky130_fd_sc_hd__dlymetal6s6s_1
x32 net35 VSS VSS VDD VDD LOAD_D sky130_fd_sc_hd__dlymetal6s6s_1
x46 net36 VSS VSS VDD VDD EN_VCM_SW_O sky130_fd_sc_hd__inv_4
x49 COUNTER[0] SAMPLE VSS VSS VDD VDD net36 sky130_fd_sc_hd__nor2_2
x52 COMP_DECIDED EN_OFFSET_CAL VSS VSS VDD VDD FINISH sky130_fd_sc_hd__nand2b_1
x51 EN_OFFSET_CAL COUNTER[0] VSS VSS VDD VDD net13 sky130_fd_sc_hd__nand2b_1
x53 COUNTER[0] EN_OFFSET_CAL VSS VSS VDD VDD net37 sky130_fd_sc_hd__nand2_2
x54 net37 VSS VSS VDD VDD OFFSET_CAL_CYCLE sky130_fd_sc_hd__inv_4
x55 RST_Zi EN_OFFSET_CAL VSS VSS VDD VDD net38 sky130_fd_sc_hd__nand2_1
x56 net38 VSS VSS VDD VDD EN_OFFSET_CAL_O sky130_fd_sc_hd__inv_2
x57 net15 VSS VSS VDD VDD LO sky130_fd_sc_hd__inv_4
x58 net14 VSS VSS VDD VDD HI sky130_fd_sc_hd__inv_4
x13[5] RESULT_Z[11] RESULT_Z[5] net16 VSS VSS VDD VDD net39[5] sky130_fd_sc_hd__mux2_1
x13[4] RESULT_Z[10] RESULT_Z[4] net16 VSS VSS VDD VDD net39[4] sky130_fd_sc_hd__mux2_1
x13[3] RESULT_Z[9] RESULT_Z[3] net16 VSS VSS VDD VDD net39[3] sky130_fd_sc_hd__mux2_1
x13[2] RESULT_Z[8] RESULT_Z[2] net16 VSS VSS VDD VDD net39[2] sky130_fd_sc_hd__mux2_1
x13[1] RESULT_Z[7] RESULT_Z[1] net16 VSS VSS VDD VDD net39[1] sky130_fd_sc_hd__mux2_1
x13[0] RESULT_Z[6] RESULT_Z[0] net16 VSS VSS VDD VDD net39[0] sky130_fd_sc_hd__mux2_1
x19 net40 VSS VSS VDD VDD net41 sky130_fd_sc_hd__inv_4
x35 COUNTER[5] VSS VSS VDD VDD net40 sky130_fd_sc_hd__inv_2
x59 COUNTER[4] DONE VSS VSS VDD VDD net16 sky130_fd_sc_hd__or2_1
x60[5] net42[5] VSS VSS VDD VDD net43[5] sky130_fd_sc_hd__inv_4
x60[4] net42[4] VSS VSS VDD VDD net43[4] sky130_fd_sc_hd__inv_4
x60[3] net42[3] VSS VSS VDD VDD net43[3] sky130_fd_sc_hd__inv_4
x60[2] net42[2] VSS VSS VDD VDD net43[2] sky130_fd_sc_hd__inv_4
x60[1] net42[1] VSS VSS VDD VDD net43[1] sky130_fd_sc_hd__inv_4
x60[0] net42[0] VSS VSS VDD VDD net43[0] sky130_fd_sc_hd__inv_4
x61[5] net39[5] VSS VSS VDD VDD net42[5] sky130_fd_sc_hd__inv_2
x61[4] net39[4] VSS VSS VDD VDD net42[4] sky130_fd_sc_hd__inv_2
x61[3] net39[3] VSS VSS VDD VDD net42[3] sky130_fd_sc_hd__inv_2
x61[2] net39[2] VSS VSS VDD VDD net42[2] sky130_fd_sc_hd__inv_2
x61[1] net39[1] VSS VSS VDD VDD net42[1] sky130_fd_sc_hd__inv_2
x61[0] net39[0] VSS VSS VDD VDD net42[0] sky130_fd_sc_hd__inv_2
x62 RSTi SAMPLE VSS VSS VDD VDD RST_RES_REG_Z sky130_fd_sc_hd__nor2_2
x33 SAMPLE IDLE CONVERT CLK_PULSE DEBUG_MUX[0] DEBUG_MUX[1] VSS VSS VDD VDD net17
+ sky130_fd_sc_hd__mux4_1
x34 CLK_COUNTER_Z EN_COMP SAMPLE_D DAC_SETTLE DEBUG_MUX[0] DEBUG_MUX[1] VSS VSS VDD VDD net18
+ sky130_fd_sc_hd__mux4_1
x42 net17 net18 net20 net21 DEBUG_MUX[2] DEBUG_MUX[3] VSS VSS VDD VDD net19 sky130_fd_sc_hd__mux4_4
x50 DAC_SETTLE_D COMP_DECIDED COMP_P COMP_N DEBUG_MUX[0] DEBUG_MUX[1] VSS VSS VDD VDD net20
+ sky130_fd_sc_hd__mux4_1
x60 DONE COUNTER[11] COUNTER[5] COUNTER[0] DEBUG_MUX[0] DEBUG_MUX[1] VSS VSS VDD VDD net21
+ sky130_fd_sc_hd__mux4_1
x43 SAMPLE EN_VCM_SW_O VSS VSS VDD VDD net22 sky130_fd_sc_hd__or2_1
x61 IDLE VSS VSS VDD VDD net23 sky130_fd_sc_hd__inv_1
x63 net19 VSS VSS VDD VDD net25 sky130_fd_sc_hd__inv_8
x64 net25 VSS VSS VDD VDD DEBUG_OUT sky130_fd_sc_hd__inv_16
x6[5] net43[5] VSS VSS VDD VDD net44[5] sky130_fd_sc_hd__inv_8
x6[4] net43[4] VSS VSS VDD VDD net44[4] sky130_fd_sc_hd__inv_8
x6[3] net43[3] VSS VSS VDD VDD net44[3] sky130_fd_sc_hd__inv_8
x6[2] net43[2] VSS VSS VDD VDD net44[2] sky130_fd_sc_hd__inv_8
x6[1] net43[1] VSS VSS VDD VDD net44[1] sky130_fd_sc_hd__inv_8
x6[0] net43[0] VSS VSS VDD VDD net44[0] sky130_fd_sc_hd__inv_8
x14[5] net44[5] VSS VSS VDD VDD DATA[5] sky130_fd_sc_hd__inv_16
x14[4] net44[4] VSS VSS VDD VDD DATA[4] sky130_fd_sc_hd__inv_16
x14[3] net44[3] VSS VSS VDD VDD DATA[3] sky130_fd_sc_hd__inv_16
x14[2] net44[2] VSS VSS VDD VDD DATA[2] sky130_fd_sc_hd__inv_16
x14[1] net44[1] VSS VSS VDD VDD DATA[1] sky130_fd_sc_hd__inv_16
x14[0] net44[0] VSS VSS VDD VDD DATA[0] sky130_fd_sc_hd__inv_16
x65 net45 VSS VSS VDD VDD CLK_DATA sky130_fd_sc_hd__inv_16
x66 net41 VSS VSS VDD VDD net45 sky130_fd_sc_hd__inv_4
**.ends
.end
